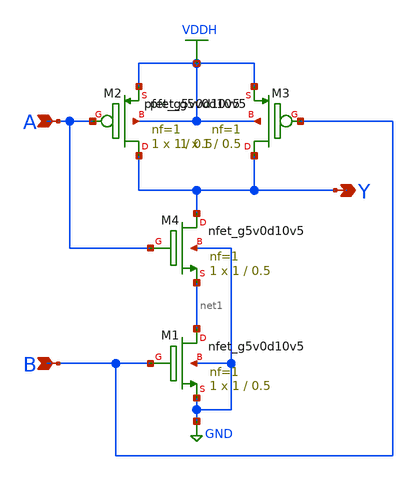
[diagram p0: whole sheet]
** sch_path: Ene_Thompson/nand2.sch
**.subckt nand2 A Y B
*.ipin A
*.opin Y
*.ipin B
XM1 net1 B GND GND sky130_fd_pr__nfet_g5v0d10v5 L=0.5 W=1 nf=1 ad='int((nf+1)/2) * W/nf * 0.29' as='int((nf+2)/2) * W/nf * 0.29'
+ pd='2*int((nf+1)/2) * (W/nf + 0.29)' ps='2*int((nf+2)/2) * (W/nf + 0.29)' nrd='0.29 / W' nrs='0.29 / W'
+ sa=0 sb=0 sd=0 mult=1 m=1
XM2 Y A VDDH VDDH sky130_fd_pr__pfet_g5v0d10v5 L=0.5 W=1 nf=1 ad='int((nf+1)/2) * W/nf * 0.29' as='int((nf+2)/2) * W/nf * 0.29'
+ pd='2*int((nf+1)/2) * (W/nf + 0.29)' ps='2*int((nf+2)/2) * (W/nf + 0.29)' nrd='0.29 / W' nrs='0.29 / W'
+ sa=0 sb=0 sd=0 mult=1 m=1
XM3 Y B VDDH VDDH sky130_fd_pr__pfet_g5v0d10v5 L=0.5 W=1 nf=1 ad='int((nf+1)/2) * W/nf * 0.29' as='int((nf+2)/2) * W/nf * 0.29'
+ pd='2*int((nf+1)/2) * (W/nf + 0.29)' ps='2*int((nf+2)/2) * (W/nf + 0.29)' nrd='0.29 / W' nrs='0.29 / W'
+ sa=0 sb=0 sd=0 mult=1 m=1
XM4 Y A net1 GND sky130_fd_pr__nfet_g5v0d10v5 L=0.5 W=1 nf=1 ad='int((nf+1)/2) * W/nf * 0.29' as='int((nf+2)/2) * W/nf * 0.29'
+ pd='2*int((nf+1)/2) * (W/nf + 0.29)' ps='2*int((nf+2)/2) * (W/nf + 0.29)' nrd='0.29 / W' nrs='0.29 / W'
+ sa=0 sb=0 sd=0 mult=1 m=1
**.ends
.GLOBAL VDDH
.GLOBAL GND
.end
